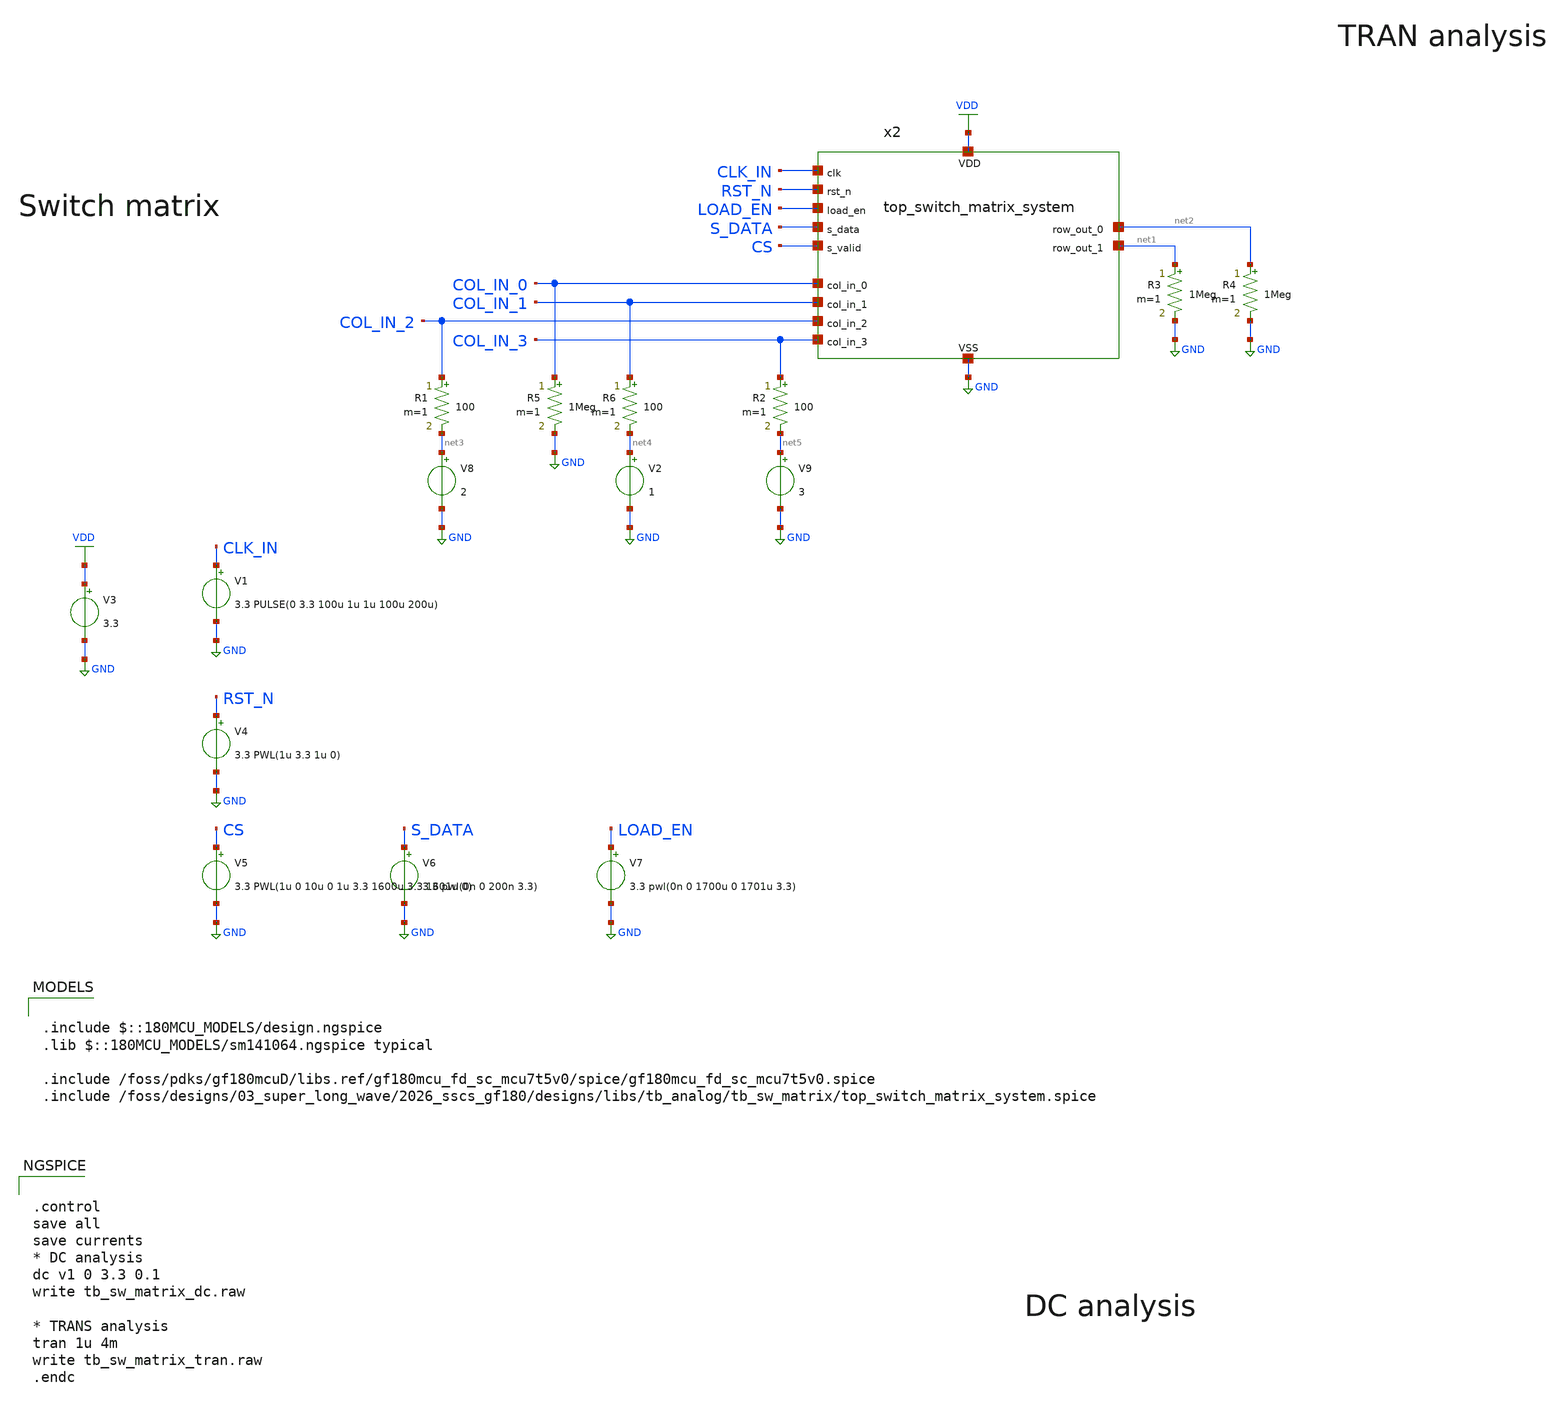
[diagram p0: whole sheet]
** sch_path: designs/libs/tb_analog/tb_sw_matrix/tb_sw_matrix.sch
* Copyright 2022 GlobalFoundries PDK Authors
* Licensed under the Apache License, Version 2.0 (the "License");
* you may not use this file except in compliance with the License.
* You may obtain a copy of the License at
* https://www.apache.org/licenses/LICENSE-2.0
* Unless required by applicable law or agreed to in writing, software
* distributed under the License is distributed on an "AS IS" BASIS,
* WITHOUT WARRANTIES OR CONDITIONS OF ANY KIND, either express or implied.
* See the License for the specific language governing permissions and
* limitations under the License.
**.subckt tb_sw_matrix
V1 CLK_IN GND 3.3 PULSE(0 3.3 100u 1u 1u 100u 200u)
V3 VDD GND 3.3
x2 VDD GND CLK_IN COL_IN_0 COL_IN_1 COL_IN_2 COL_IN_3 LOAD_EN net2 net1 RST_N S_DATA CS
+ top_switch_matrix_system
R3 net1 GND 1Meg m=1
R4 net2 GND 1Meg m=1
V4 RST_N GND 3.3 PWL(1u 3.3 1u 0)
V5 CS GND 3.3 PWL(1u 0 10u 0 1u 3.3 1600u 3.3 1601u 0)
V6 S_DATA GND 3.3 pwl(0n 0 200n 3.3)
V7 LOAD_EN GND 3.3 pwl(0n 0 1700u 0 1701u 3.3)
R1 COL_IN_2 net3 100 m=1
R5 COL_IN_0 GND 1Meg m=1
R6 COL_IN_1 net4 100 m=1
V2 net4 GND 1
V8 net3 GND 2
R2 COL_IN_3 net5 100 m=1
V9 net5 GND 3
**** begin user architecture code

.include $::180MCU_MODELS/design.ngspice
.lib $::180MCU_MODELS/sm141064.ngspice typical

.include /foss/pdks/gf180mcuD/libs.ref/gf180mcu_fd_sc_mcu7t5v0/spice/gf180mcu_fd_sc_mcu7t5v0.spice
.include /foss/designs/03_super_long_wave/2026_sscs_gf180/designs/libs/tb_analog/tb_sw_matrix/top_switch_matrix_system.spice



.control
save all
save currents
* DC analysis
dc v1 0 3.3 0.1
write tb_sw_matrix_dc.raw

* TRANS analysis
tran 1u 4m
write tb_sw_matrix_tran.raw
.endc


**** end user architecture code
**.ends
.GLOBAL GND
.GLOBAL VDD
.end
